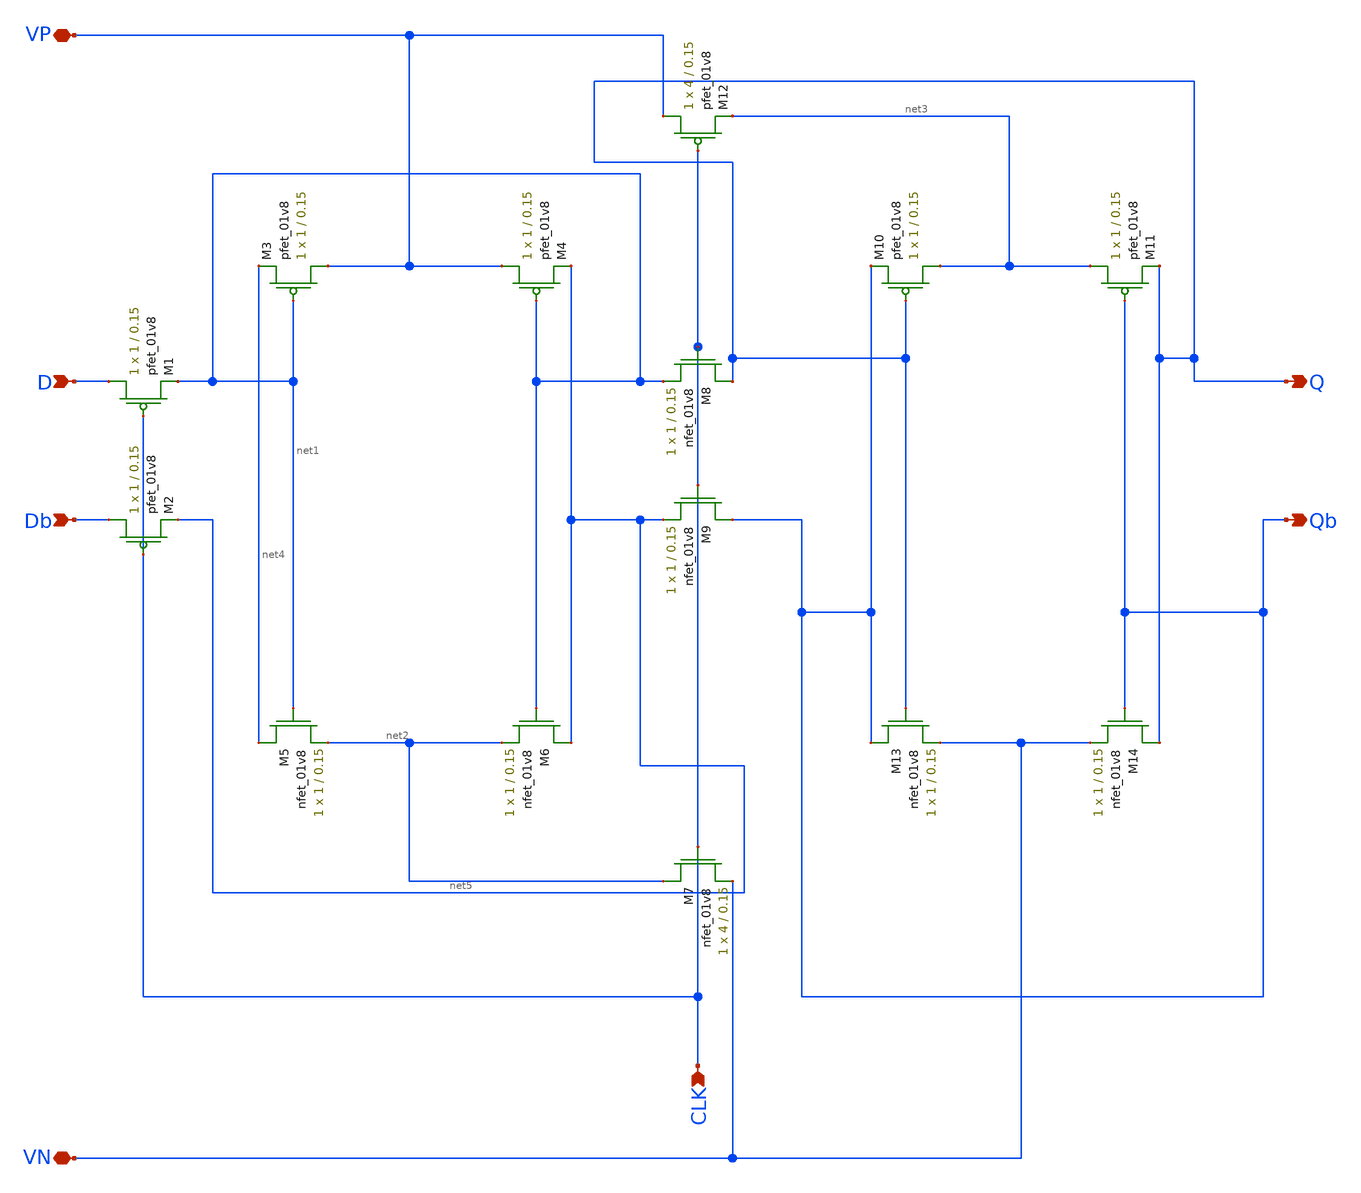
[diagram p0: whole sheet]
** sch_path: simulation/shift_register/andrew_mp2_files/d_flipflop/d_flipflop_LDS_v3.sch
**.subckt d_flipflop_LDS_v3 D CLK Q Qb Db VP VN
*.ipin D
*.ipin CLK
*.opin Q
*.opin Qb
*.ipin Db
*.iopin VP
*.iopin VN
XM1 D CLK net1 VDD sky130_fd_pr__pfet_01v8 L=0.15 W=1 nf=1 ad='int((nf+1)/2) * W/nf * 0.29' as='int((nf+2)/2) * W/nf * 0.29'
+ pd='2*int((nf+1)/2) * (W/nf + 0.29)' ps='2*int((nf+2)/2) * (W/nf + 0.29)' nrd='0.29 / W' nrs='0.29 / W'
+ sa=0 sb=0 sd=0 mult=1 m=1
XM2 Db CLK net5 VDD sky130_fd_pr__pfet_01v8 L=0.15 W=1 nf=1 ad='int((nf+1)/2) * W/nf * 0.29' as='int((nf+2)/2) * W/nf * 0.29'
+ pd='2*int((nf+1)/2) * (W/nf + 0.29)' ps='2*int((nf+2)/2) * (W/nf + 0.29)' nrd='0.29 / W' nrs='0.29 / W'
+ sa=0 sb=0 sd=0 mult=1 m=1
XM3 VP net1 net4 VDD sky130_fd_pr__pfet_01v8 L=0.15 W=1 nf=1 ad='int((nf+1)/2) * W/nf * 0.29' as='int((nf+2)/2) * W/nf * 0.29'
+ pd='2*int((nf+1)/2) * (W/nf + 0.29)' ps='2*int((nf+2)/2) * (W/nf + 0.29)' nrd='0.29 / W' nrs='0.29 / W'
+ sa=0 sb=0 sd=0 mult=1 m=1
XM5 net4 net1 net2 GND sky130_fd_pr__nfet_01v8 L=0.15 W=1 nf=1 ad='int((nf+1)/2) * W/nf * 0.29' as='int((nf+2)/2) * W/nf * 0.29'
+ pd='2*int((nf+1)/2) * (W/nf + 0.29)' ps='2*int((nf+2)/2) * (W/nf + 0.29)' nrd='0.29 / W' nrs='0.29 / W'
+ sa=0 sb=0 sd=0 mult=1 m=1
XM7 net2 CLK VN GND sky130_fd_pr__nfet_01v8 L=0.15 W=4 nf=1 ad='int((nf+1)/2) * W/nf * 0.29' as='int((nf+2)/2) * W/nf * 0.29'
+ pd='2*int((nf+1)/2) * (W/nf + 0.29)' ps='2*int((nf+2)/2) * (W/nf + 0.29)' nrd='0.29 / W' nrs='0.29 / W'
+ sa=0 sb=0 sd=0 mult=1 m=1
XM8 Q CLK net1 GND sky130_fd_pr__nfet_01v8 L=0.15 W=1 nf=1 ad='int((nf+1)/2) * W/nf * 0.29' as='int((nf+2)/2) * W/nf * 0.29'
+ pd='2*int((nf+1)/2) * (W/nf + 0.29)' ps='2*int((nf+2)/2) * (W/nf + 0.29)' nrd='0.29 / W' nrs='0.29 / W'
+ sa=0 sb=0 sd=0 mult=1 m=1
XM9 Qb CLK net5 GND sky130_fd_pr__nfet_01v8 L=0.15 W=1 nf=1 ad='int((nf+1)/2) * W/nf * 0.29' as='int((nf+2)/2) * W/nf * 0.29'
+ pd='2*int((nf+1)/2) * (W/nf + 0.29)' ps='2*int((nf+2)/2) * (W/nf + 0.29)' nrd='0.29 / W' nrs='0.29 / W'
+ sa=0 sb=0 sd=0 mult=1 m=1
XM10 net3 Q Qb VDD sky130_fd_pr__pfet_01v8 L=0.15 W=1 nf=1 ad='int((nf+1)/2) * W/nf * 0.29' as='int((nf+2)/2) * W/nf * 0.29'
+ pd='2*int((nf+1)/2) * (W/nf + 0.29)' ps='2*int((nf+2)/2) * (W/nf + 0.29)' nrd='0.29 / W' nrs='0.29 / W'
+ sa=0 sb=0 sd=0 mult=1 m=1
XM11 net3 Qb Q VDD sky130_fd_pr__pfet_01v8 L=0.15 W=1 nf=1 ad='int((nf+1)/2) * W/nf * 0.29' as='int((nf+2)/2) * W/nf * 0.29'
+ pd='2*int((nf+1)/2) * (W/nf + 0.29)' ps='2*int((nf+2)/2) * (W/nf + 0.29)' nrd='0.29 / W' nrs='0.29 / W'
+ sa=0 sb=0 sd=0 mult=1 m=1
XM12 VP CLK net3 VDD sky130_fd_pr__pfet_01v8 L=0.15 W=4 nf=1 ad='int((nf+1)/2) * W/nf * 0.29' as='int((nf+2)/2) * W/nf * 0.29'
+ pd='2*int((nf+1)/2) * (W/nf + 0.29)' ps='2*int((nf+2)/2) * (W/nf + 0.29)' nrd='0.29 / W' nrs='0.29 / W'
+ sa=0 sb=0 sd=0 mult=1 m=1
XM13 Qb Q VN GND sky130_fd_pr__nfet_01v8 L=0.15 W=1 nf=1 ad='int((nf+1)/2) * W/nf * 0.29' as='int((nf+2)/2) * W/nf * 0.29'
+ pd='2*int((nf+1)/2) * (W/nf + 0.29)' ps='2*int((nf+2)/2) * (W/nf + 0.29)' nrd='0.29 / W' nrs='0.29 / W'
+ sa=0 sb=0 sd=0 mult=1 m=1
XM14 Q Qb VN GND sky130_fd_pr__nfet_01v8 L=0.15 W=1 nf=1 ad='int((nf+1)/2) * W/nf * 0.29' as='int((nf+2)/2) * W/nf * 0.29'
+ pd='2*int((nf+1)/2) * (W/nf + 0.29)' ps='2*int((nf+2)/2) * (W/nf + 0.29)' nrd='0.29 / W' nrs='0.29 / W'
+ sa=0 sb=0 sd=0 mult=1 m=1
XM4 VP net1 net5 VDD sky130_fd_pr__pfet_01v8 L=0.15 W=1 nf=1 ad='int((nf+1)/2) * W/nf * 0.29' as='int((nf+2)/2) * W/nf * 0.29'
+ pd='2*int((nf+1)/2) * (W/nf + 0.29)' ps='2*int((nf+2)/2) * (W/nf + 0.29)' nrd='0.29 / W' nrs='0.29 / W'
+ sa=0 sb=0 sd=0 mult=1 m=1
XM6 net5 net1 net2 GND sky130_fd_pr__nfet_01v8 L=0.15 W=1 nf=1 ad='int((nf+1)/2) * W/nf * 0.29' as='int((nf+2)/2) * W/nf * 0.29'
+ pd='2*int((nf+1)/2) * (W/nf + 0.29)' ps='2*int((nf+2)/2) * (W/nf + 0.29)' nrd='0.29 / W' nrs='0.29 / W'
+ sa=0 sb=0 sd=0 mult=1 m=1
**.ends
.end
